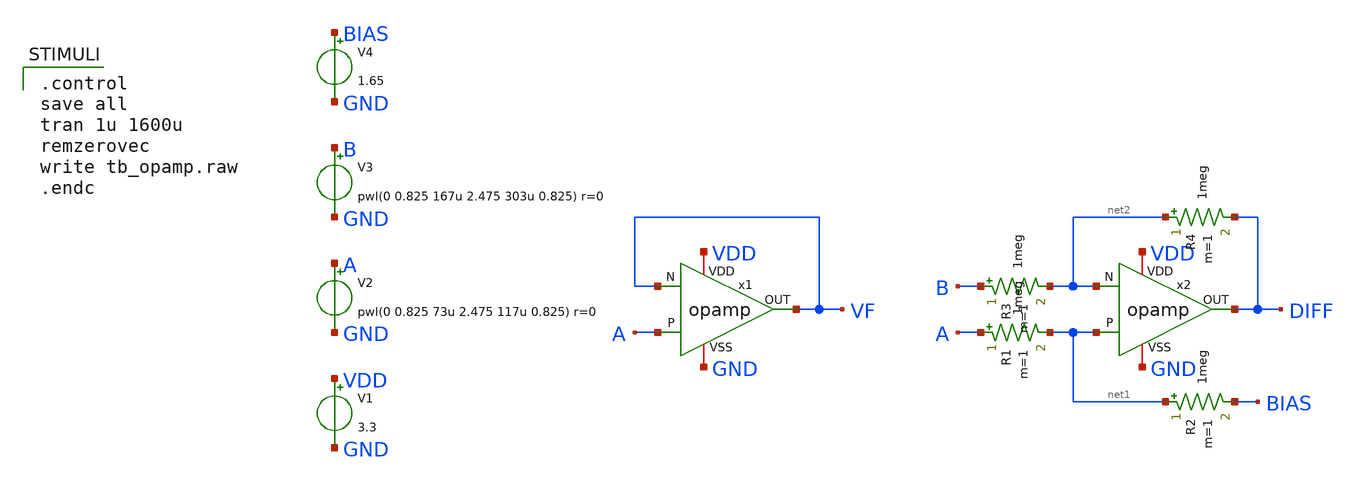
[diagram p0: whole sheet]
** sch_path: xschem/tb_opamp.sch
**.subckt tb_opamp
V1 VDD GND 3.3
V2 A GND pwl(0 0.825 73u 2.475 117u 0.825) r=0
V3 B GND pwl(0 0.825 167u 2.475 303u 0.825) r=0
x1 VDD VF A VF GND opamp
x2 VDD DIFF net1 net2 GND opamp
R1 A net1 1meg m=1
R2 net1 BIAS 1meg m=1
R3 B net2 1meg m=1
R4 net2 DIFF 1meg m=1
V4 BIAS GND 1.65
**** begin user architecture code

.control
save all
tran 1u 1600u
remzerovec
write tb_opamp.raw
.endc


 .lib $::SKYWATER_MODELS/sky130.lib.spice tt
.include $::SKYWATER_STDCELLS/sky130_fd_sc_hd.spice

**** end user architecture code
**.ends

* expanding   symbol:  opamp.sym # of pins=5
** sym_path: xschem/opamp.sym
** sch_path: xschem/opamp.sch
.subckt opamp VDD OUT P N VSS
*.iopin VDD
*.iopin VSS
*.ipin P
*.ipin N
*.opin OUT
XR1 net2 VDD VSS sky130_fd_pr__res_xhigh_po_0p35 L=25 mult=1 m=1
XM1 net2 net2 VSS VSS sky130_fd_pr__nfet_g5v0d10v5 L=1 W=2 nf=1 ad='int((1 + 1)/2) * 2 / 1 * 0.29' as='int((1 + 2)/2) * 2 / 1 * 0.29'
+ pd='2*int((1 + 1)/2) * (2 / 1 + 0.29)' ps='2*int((1 + 2)/2) * (2 / 1 + 0.29)' nrd='0.29 / 2 ' nrs='0.29 / 2 '
+ sa=0 sb=0 sd=0 mult=2 m=2
XM7 net1 net1 VDD VDD sky130_fd_pr__pfet_g5v0d10v5 L=1 W=4 nf=1 ad='int((1 + 1)/2) * 4 / 1 * 0.29' as='int((1 + 2)/2) * 4 / 1 * 0.29'
+ pd='2*int((1 + 1)/2) * (4 / 1 + 0.29)' ps='2*int((1 + 2)/2) * (4 / 1 + 0.29)' nrd='0.29 / 4 ' nrs='0.29 / 4 '
+ sa=0 sb=0 sd=0 mult=2 m=2
XM8 OUT net1 VDD VDD sky130_fd_pr__pfet_g5v0d10v5 L=1 W=4 nf=1 ad='int((1 + 1)/2) * 4 / 1 * 0.29' as='int((1 + 2)/2) * 4 / 1 * 0.29'
+ pd='2*int((1 + 1)/2) * (4 / 1 + 0.29)' ps='2*int((1 + 2)/2) * (4 / 1 + 0.29)' nrd='0.29 / 4 ' nrs='0.29 / 4 '
+ sa=0 sb=0 sd=0 mult=2 m=2
XM4 net6 net2 VSS VSS sky130_fd_pr__nfet_g5v0d10v5 L=1 W=2 nf=1 ad='int((1 + 1)/2) * 2 / 1 * 0.29' as='int((1 + 2)/2) * 2 / 1 * 0.29'
+ pd='2*int((1 + 1)/2) * (2 / 1 + 0.29)' ps='2*int((1 + 2)/2) * (2 / 1 + 0.29)' nrd='0.29 / 2 ' nrs='0.29 / 2 '
+ sa=0 sb=0 sd=0 mult=2 m=2
XM5 net1 P net6 VSS sky130_fd_pr__nfet_g5v0d10v5 L=1 W=2 nf=1 ad='int((1 + 1)/2) * 2 / 1 * 0.29' as='int((1 + 2)/2) * 2 / 1 * 0.29'
+ pd='2*int((1 + 1)/2) * (2 / 1 + 0.29)' ps='2*int((1 + 2)/2) * (2 / 1 + 0.29)' nrd='0.29 / 2 ' nrs='0.29 / 2 '
+ sa=0 sb=0 sd=0 mult=2 m=2
XM6 OUT N net6 VSS sky130_fd_pr__nfet_g5v0d10v5 L=1 W=2 nf=1 ad='int((1 + 1)/2) * 2 / 1 * 0.29' as='int((1 + 2)/2) * 2 / 1 * 0.29'
+ pd='2*int((1 + 1)/2) * (2 / 1 + 0.29)' ps='2*int((1 + 2)/2) * (2 / 1 + 0.29)' nrd='0.29 / 2 ' nrs='0.29 / 2 '
+ sa=0 sb=0 sd=0 mult=2 m=2
XM2 net5 net2 VSS VSS sky130_fd_pr__nfet_g5v0d10v5 L=1 W=2 nf=1 ad='int((1 + 1)/2) * 2 / 1 * 0.29' as='int((1 + 2)/2) * 2 / 1 * 0.29'
+ pd='2*int((1 + 1)/2) * (2 / 1 + 0.29)' ps='2*int((1 + 2)/2) * (2 / 1 + 0.29)' nrd='0.29 / 2 ' nrs='0.29 / 2 '
+ sa=0 sb=0 sd=0 mult=2 m=2
XM9 net4 net5 VDD VDD sky130_fd_pr__pfet_g5v0d10v5 L=1 W=4 nf=1 ad='int((1 + 1)/2) * 4 / 1 * 0.29' as='int((1 + 2)/2) * 4 / 1 * 0.29'
+ pd='2*int((1 + 1)/2) * (4 / 1 + 0.29)' ps='2*int((1 + 2)/2) * (4 / 1 + 0.29)' nrd='0.29 / 4 ' nrs='0.29 / 4 '
+ sa=0 sb=0 sd=0 mult=2 m=2
XM3 VDD net5 net5 VDD sky130_fd_pr__pfet_g5v0d10v5 L=1 W=4 nf=1 ad='int((1 + 1)/2) * 4 / 1 * 0.29' as='int((1 + 2)/2) * 4 / 1 * 0.29'
+ pd='2*int((1 + 1)/2) * (4 / 1 + 0.29)' ps='2*int((1 + 2)/2) * (4 / 1 + 0.29)' nrd='0.29 / 4 ' nrs='0.29 / 4 '
+ sa=0 sb=0 sd=0 mult=2 m=2
XM10 net3 P net4 VDD sky130_fd_pr__pfet_g5v0d10v5 L=1 W=4 nf=1 ad='int((1 + 1)/2) * 4 / 1 * 0.29' as='int((1 + 2)/2) * 4 / 1 * 0.29'
+ pd='2*int((1 + 1)/2) * (4 / 1 + 0.29)' ps='2*int((1 + 2)/2) * (4 / 1 + 0.29)' nrd='0.29 / 4 ' nrs='0.29 / 4 '
+ sa=0 sb=0 sd=0 mult=2 m=2
XM11 OUT N net4 VDD sky130_fd_pr__pfet_g5v0d10v5 L=1 W=4 nf=1 ad='int((1 + 1)/2) * 4 / 1 * 0.29' as='int((1 + 2)/2) * 4 / 1 * 0.29'
+ pd='2*int((1 + 1)/2) * (4 / 1 + 0.29)' ps='2*int((1 + 2)/2) * (4 / 1 + 0.29)' nrd='0.29 / 4 ' nrs='0.29 / 4 '
+ sa=0 sb=0 sd=0 mult=2 m=2
XM12 net3 net3 VSS VSS sky130_fd_pr__nfet_g5v0d10v5 L=1 W=2 nf=1 ad='int((1 + 1)/2) * 2 / 1 * 0.29' as='int((1 + 2)/2) * 2 / 1 * 0.29'
+ pd='2*int((1 + 1)/2) * (2 / 1 + 0.29)' ps='2*int((1 + 2)/2) * (2 / 1 + 0.29)' nrd='0.29 / 2 ' nrs='0.29 / 2 '
+ sa=0 sb=0 sd=0 mult=2 m=2
XM13 OUT net3 VSS VSS sky130_fd_pr__nfet_g5v0d10v5 L=1 W=2 nf=1 ad='int((1 + 1)/2) * 2 / 1 * 0.29' as='int((1 + 2)/2) * 2 / 1 * 0.29'
+ pd='2*int((1 + 1)/2) * (2 / 1 + 0.29)' ps='2*int((1 + 2)/2) * (2 / 1 + 0.29)' nrd='0.29 / 2 ' nrs='0.29 / 2 '
+ sa=0 sb=0 sd=0 mult=2 m=2
.ends

.end
